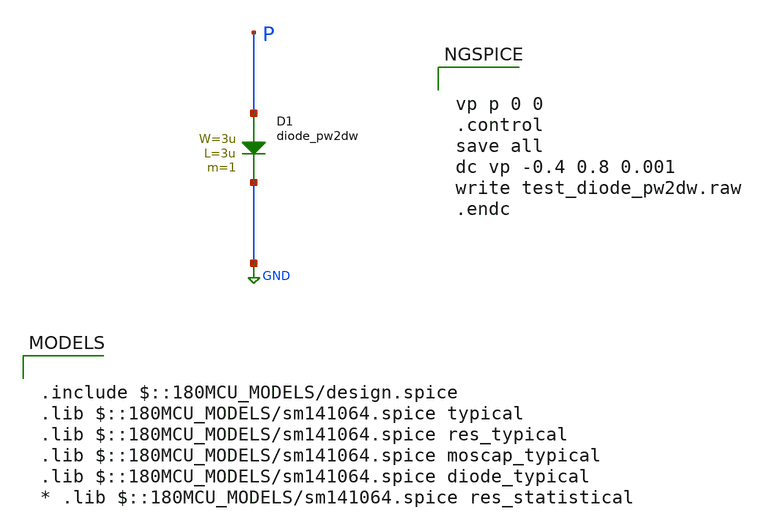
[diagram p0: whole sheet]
** sch_path: cells/xschem/tests/test_diode_pw2dw.sch
* Copyright 2022 GlobalFoundries PDK Authors
* Licensed under the Apache License, Version 2.0 (the "License");
* you may not use this file except in compliance with the License.
* You may obtain a copy of the License at
* https://www.apache.org/licenses/LICENSE-2.0
* Unless required by applicable law or agreed to in writing, software
* distributed under the License is distributed on an "AS IS" BASIS,
* WITHOUT WARRANTIES OR CONDITIONS OF ANY KIND, either express or implied.
* See the License for the specific language governing permissions and
* limitations under the License.
**.subckt test_diode_pw2dw
D1 P GND diode_pw2dw area='3u * 3u ' pj='2*3u + 2*3u ' m=1
**** begin user architecture code

.include $::180MCU_MODELS/design.spice
.lib $::180MCU_MODELS/sm141064.spice typical
.lib $::180MCU_MODELS/sm141064.spice res_typical
.lib $::180MCU_MODELS/sm141064.spice moscap_typical
.lib $::180MCU_MODELS/sm141064.spice diode_typical
* .lib $::180MCU_MODELS/sm141064.spice res_statistical



vp p 0 0
.control
save all
dc vp -0.4 0.8 0.001
write test_diode_pw2dw.raw
.endc


**** end user architecture code
**.ends
.GLOBAL GND
.end
